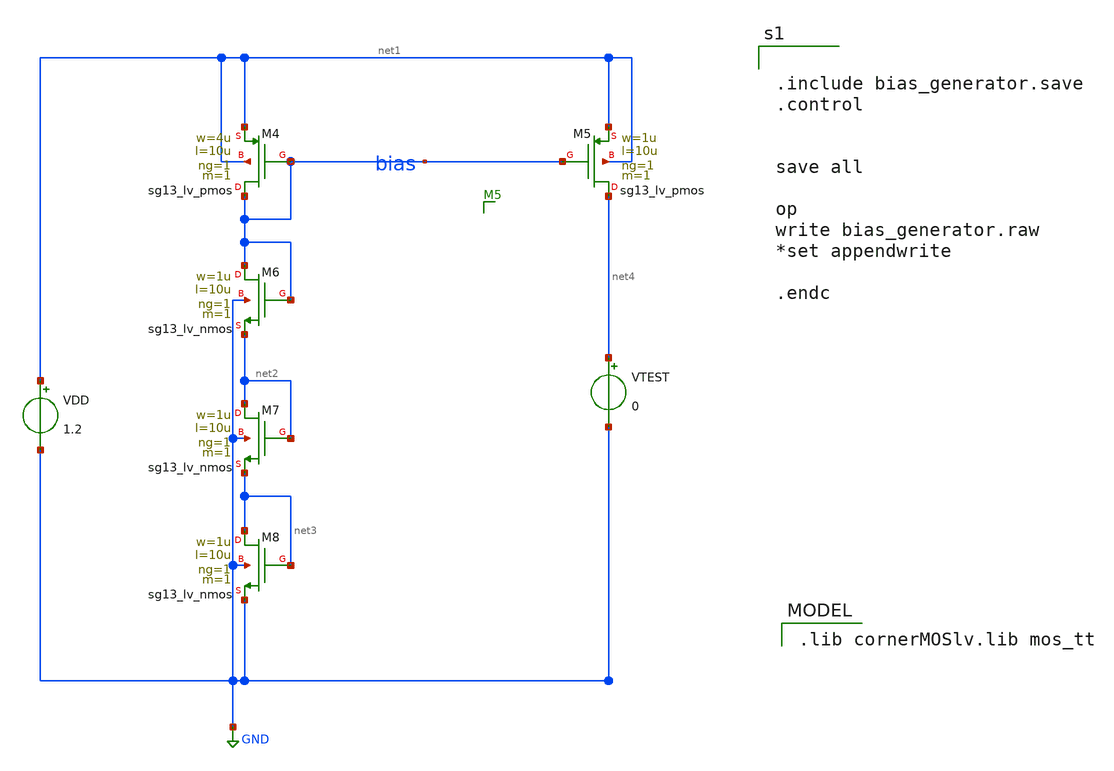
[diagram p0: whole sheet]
** sch_path: bias_generator.sch
**.subckt bias_generator
XM4 bias bias net1 net1 sg13_lv_pmos w=4u l=10u ng=1 m=1 mm_ok=1
XM6 bias bias net2 GND sg13_lv_nmos w=1u l=10u ng=1 m=1 mm_ok=1
XM7 net2 net2 net3 GND sg13_lv_nmos w=1u l=10u ng=1 m=1 mm_ok=1
XM8 net3 net3 GND GND sg13_lv_nmos w=1u l=10u ng=1 m=1 mm_ok=1
VDD net1 GND 1.2
XM5 net4 bias net1 net1 sg13_lv_pmos w=1u l=10u ng=1 m=1 mm_ok=1
VTEST net4 GND 0
**** begin user architecture code
 .lib cornerMOSlv.lib mos_tt



.include bias_generator.save
.control


save all

op
write bias_generator.raw
*set appendwrite

.endc


**** end user architecture code
**.ends
.GLOBAL GND
.end
